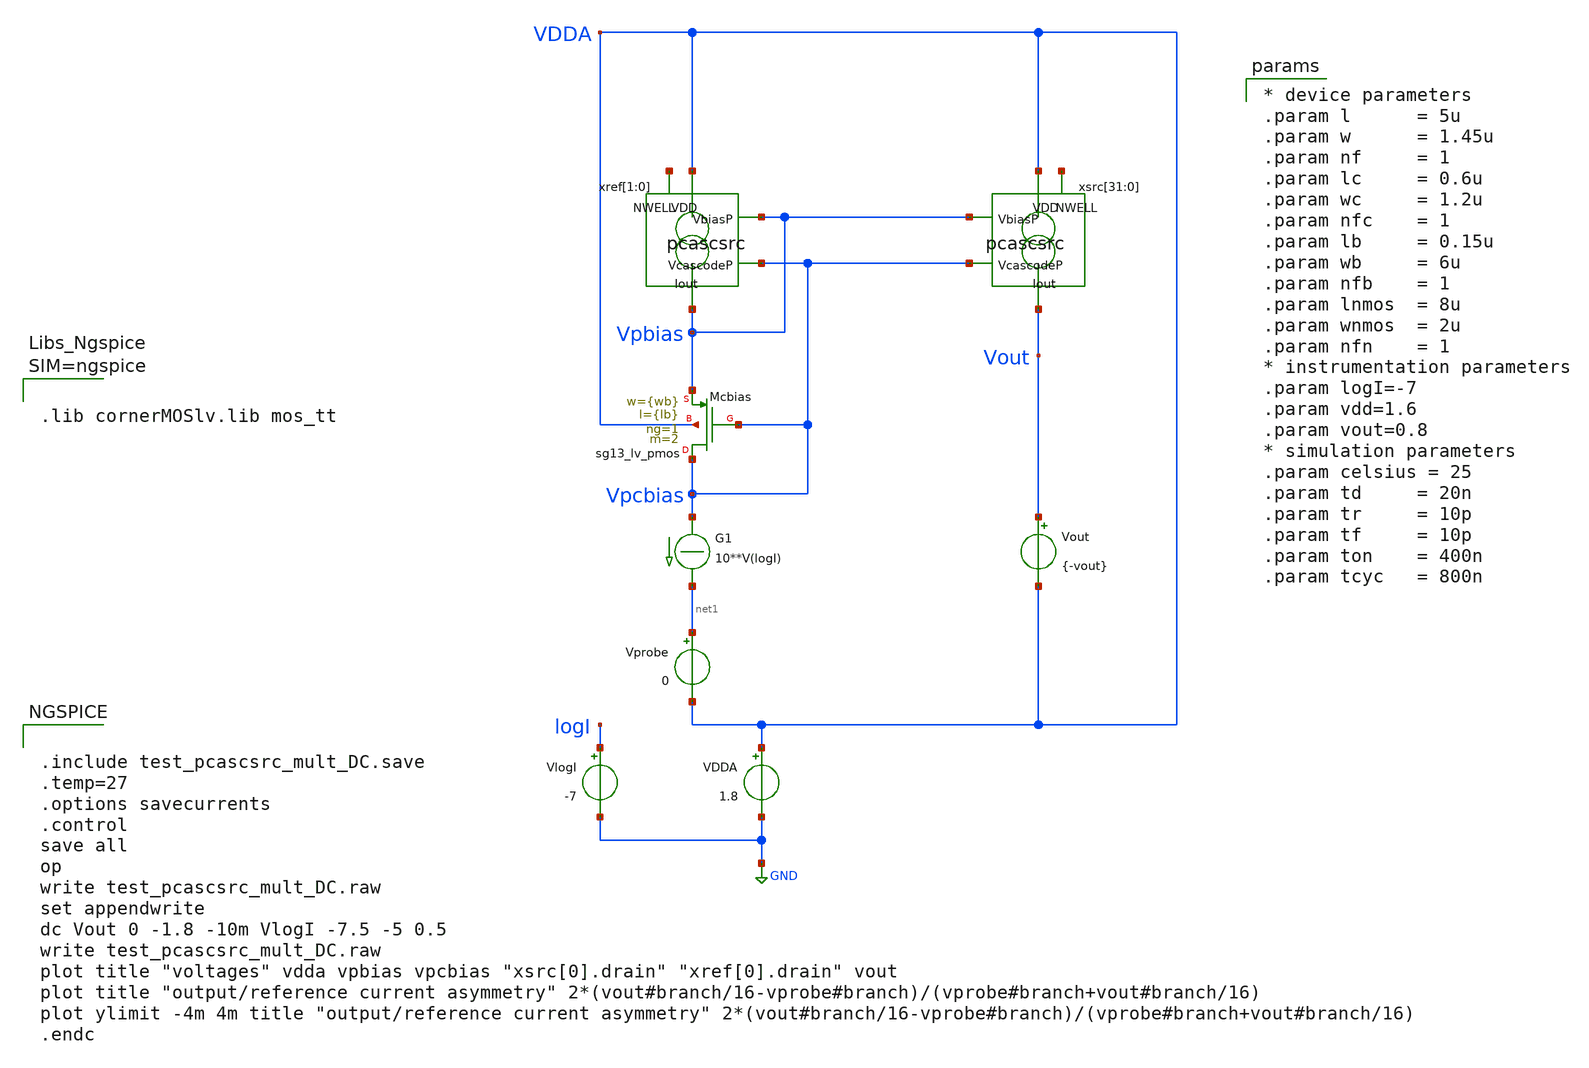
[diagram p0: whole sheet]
** sch_path: xschem/test_pcascsrc_mult_DC.sch
**.subckt test_pcascsrc_mult_DC
Vout Vout VDDA {-vout}
.save i(vout)
Vprobe net1 VDDA 0
.save i(vprobe)
G1 Vpcbias net1 CUR=' 10**V(logI) '
VlogI logI GND -7
.save i(vlogi)
xref[1] VDDA Vpbias Vpcbias Vpbias net2[1] pcascsrc
xref[0] VDDA Vpbias Vpcbias Vpbias net2[0] pcascsrc
xsrc[31] VDDA Vpbias Vpcbias Vout net3[31] pcascsrc
xsrc[30] VDDA Vpbias Vpcbias Vout net3[30] pcascsrc
xsrc[29] VDDA Vpbias Vpcbias Vout net3[29] pcascsrc
xsrc[28] VDDA Vpbias Vpcbias Vout net3[28] pcascsrc
xsrc[27] VDDA Vpbias Vpcbias Vout net3[27] pcascsrc
xsrc[26] VDDA Vpbias Vpcbias Vout net3[26] pcascsrc
xsrc[25] VDDA Vpbias Vpcbias Vout net3[25] pcascsrc
xsrc[24] VDDA Vpbias Vpcbias Vout net3[24] pcascsrc
xsrc[23] VDDA Vpbias Vpcbias Vout net3[23] pcascsrc
xsrc[22] VDDA Vpbias Vpcbias Vout net3[22] pcascsrc
xsrc[21] VDDA Vpbias Vpcbias Vout net3[21] pcascsrc
xsrc[20] VDDA Vpbias Vpcbias Vout net3[20] pcascsrc
xsrc[19] VDDA Vpbias Vpcbias Vout net3[19] pcascsrc
xsrc[18] VDDA Vpbias Vpcbias Vout net3[18] pcascsrc
xsrc[17] VDDA Vpbias Vpcbias Vout net3[17] pcascsrc
xsrc[16] VDDA Vpbias Vpcbias Vout net3[16] pcascsrc
xsrc[15] VDDA Vpbias Vpcbias Vout net3[15] pcascsrc
xsrc[14] VDDA Vpbias Vpcbias Vout net3[14] pcascsrc
xsrc[13] VDDA Vpbias Vpcbias Vout net3[13] pcascsrc
xsrc[12] VDDA Vpbias Vpcbias Vout net3[12] pcascsrc
xsrc[11] VDDA Vpbias Vpcbias Vout net3[11] pcascsrc
xsrc[10] VDDA Vpbias Vpcbias Vout net3[10] pcascsrc
xsrc[9] VDDA Vpbias Vpcbias Vout net3[9] pcascsrc
xsrc[8] VDDA Vpbias Vpcbias Vout net3[8] pcascsrc
xsrc[7] VDDA Vpbias Vpcbias Vout net3[7] pcascsrc
xsrc[6] VDDA Vpbias Vpcbias Vout net3[6] pcascsrc
xsrc[5] VDDA Vpbias Vpcbias Vout net3[5] pcascsrc
xsrc[4] VDDA Vpbias Vpcbias Vout net3[4] pcascsrc
xsrc[3] VDDA Vpbias Vpcbias Vout net3[3] pcascsrc
xsrc[2] VDDA Vpbias Vpcbias Vout net3[2] pcascsrc
xsrc[1] VDDA Vpbias Vpcbias Vout net3[1] pcascsrc
xsrc[0] VDDA Vpbias Vpcbias Vout net3[0] pcascsrc
VDDA VDDA GND 1.8
.save i(vdda)
XMcbias Vpcbias Vpcbias Vpbias VDDA sg13_lv_pmos w={wb} l={lb} ng=1 m=2 mm_ok=1
**** begin user architecture code


.include test_pcascsrc_mult_DC.save
.temp=27
.options savecurrents
.control
save all
op
write test_pcascsrc_mult_DC.raw
set appendwrite
dc Vout 0 -1.8 -10m VlogI -7.5 -5 0.5
write test_pcascsrc_mult_DC.raw
plot title "voltages" vdda vpbias vpcbias "xsrc[0].drain" "xref[0].drain" vout
plot title "output/reference current asymmetry"
+ 2*(vout#branch/16-vprobe#branch)/(vprobe#branch+vout#branch/16)
plot ylimit -4m 4m title "output/reference current asymmetry"
+ 2*(vout#branch/16-vprobe#branch)/(vprobe#branch+vout#branch/16)
.endc





.lib cornerMOSlv.lib mos_tt




* device parameters
.param l      = 5u
.param w      = 1.45u
.param nf     = 1
.param lc     = 0.6u
.param wc     = 1.2u
.param nfc    = 1
.param lb     = 0.15u
.param wb     = 6u
.param nfb    = 1
.param lnmos  = 8u
.param wnmos  = 2u
.param nfn    = 1
* instrumentation parameters
.param logI=-7
.param vdd=1.6
.param vout=0.8
* simulation parameters
.param celsius = 25
.param td     = 20n
.param tr     = 10p
.param tf     = 10p
.param ton    = 400n
.param tcyc   = 800n


**** end user architecture code
**.ends

* expanding   symbol:  pcascsrc.sym # of pins=5
** sym_path: xschem/pcascsrc.sym
** sch_path: xschem/pcascsrc.sch
.subckt pcascsrc VDD VbiasP VcascodeP Iout NWELL
*.ipin VcascodeP
*.ipin VbiasP
*.opin Iout
*.ipin VDD
*.iopin NWELL
XMsrc drain VbiasP VDD NWELL sg13_lv_pmos w=0.74u l=2u ng=1 m=1 mm_ok=1
XMcasc Iout VcascodeP drain NWELL sg13_lv_pmos w=0.3u l=0.3u ng=1 m=1 mm_ok=1
.ends

.GLOBAL GND
.end
